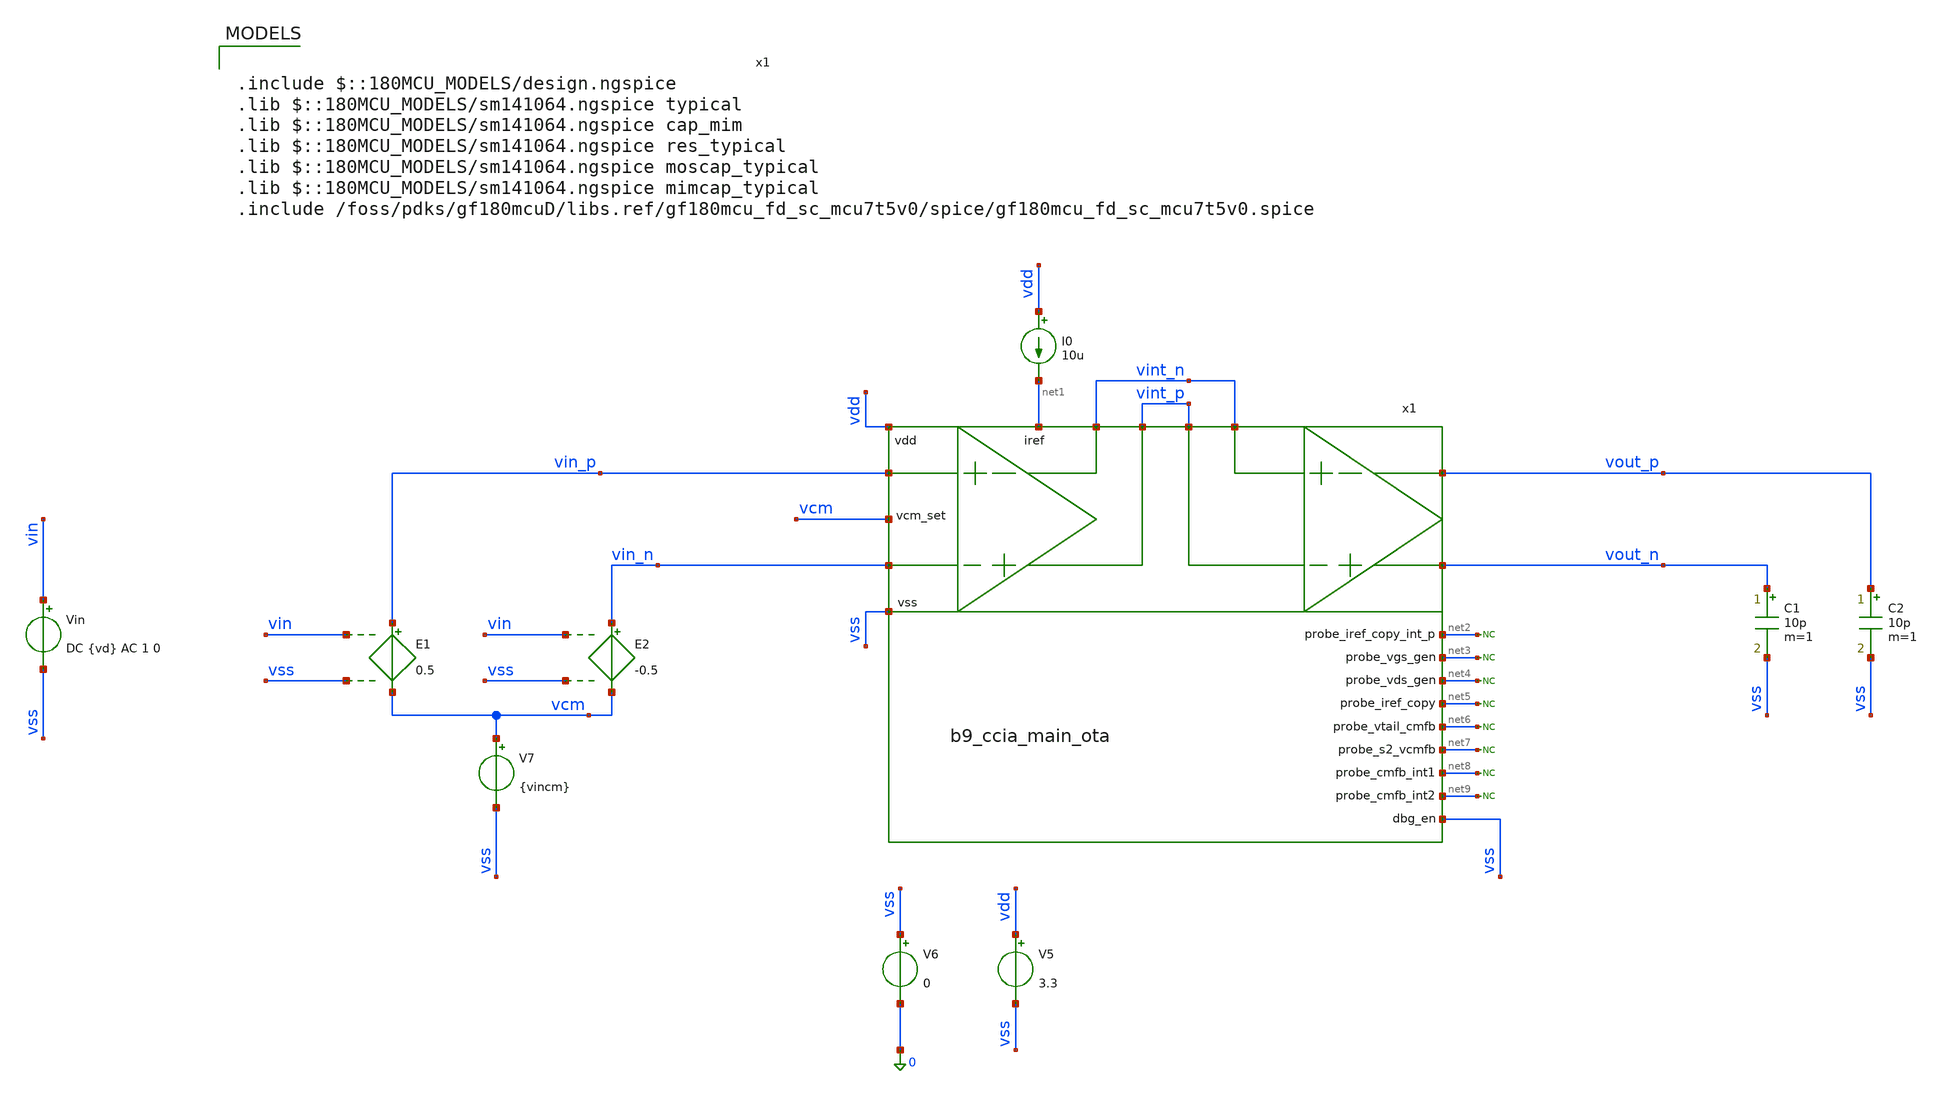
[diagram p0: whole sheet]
** sch_path: xschem/ccia_main_ota/b9_ccia_main_ota_tb_basic.sch
**.subckt b9_ccia_main_ota_tb_basic
I0 vdd net1 10u
C1 vout_n vss 10p m=1
C2 vout_p vss 10p m=1
V7 vcm vss {vincm}
E1 vin_p vcm vin vss 0.5
E2 vin_n vcm vin vss -0.5
Vin vin vss DC {vd} AC 1 0
V5 vdd vss 3.3
V6 vss 0 0
x1 net2 net3 net4 net5 net6 net7 net8 net9 vss net1 vdd vint_p vin_p vin_n vint_n vss vout_n vint_n
+ vcm vint_p vout_p b9_ccia_main_ota
* noconn #net2
* noconn #net3
* noconn #net4
* noconn #net5
* noconn #net6
* noconn #net7
* noconn #net8
* noconn #net9
**** begin user architecture code

.include $::180MCU_MODELS/design.ngspice
.lib $::180MCU_MODELS/sm141064.ngspice typical
.lib $::180MCU_MODELS/sm141064.ngspice cap_mim
.lib $::180MCU_MODELS/sm141064.ngspice res_typical
.lib $::180MCU_MODELS/sm141064.ngspice moscap_typical
.lib $::180MCU_MODELS/sm141064.ngspice mimcap_typical
.include /foss/pdks/gf180mcuD/libs.ref/gf180mcu_fd_sc_mcu7t5v0/spice/gf180mcu_fd_sc_mcu7t5v0.spice


.param vincm=1
.param voutcm=0.8
.param vd=0
.control
save all
save @m.x1.x10.x1.xm1.m0[id] @m.x1.x10.x1.xm1.m0[gm] @m.x1.x10.x1.xm1.m0[gds]
+ @m.x1.x10.x1.xm1.m0[cdb] @m.x1.x10.x1.xm1.m0[cgs] @m.x1.x10.x1.xm1.m0[csb] @m.x1.x10.x1.xm1.m0[cgd]
save @m.x1.x10.x1.xm2.m0[id] @m.x1.x10.x1.xm2.m0[gm] @m.x1.x10.x1.xm2.m0[gds]
+ @m.x1.x10.x1.xm2.m0[cdb] @m.x1.x10.x1.xm2.m0[cgs] @m.x1.x10.x1.xm2.m0[csb] @m.x1.x10.x1.xm2.m0[cgd]
save @m.x1.x10.xm1.m0[id] @m.x1.x10.xm1.m0[gm] @m.x1.x10.xm1.m0[gds] @m.x1.x10.xm1.m0[cdb]
+ @m.x1.x10.xm1.m0[cgs] @m.x1.x10.xm1.m0[csb] @m.x1.x10.xm1.m0[cgd]
save @m.x1.x12.x1.xm1.m0[id] @m.x1.x12.x1.xm1.m0[gm] @m.x1.x12.x1.xm1.m0[gds]
+ @m.x1.x12.x1.xm1.m0[cdb] @m.x1.x12.x1.xm1.m0[cgs] @m.x1.x12.x1.xm1.m0[csb] @m.x1.x12.x1.xm1.m0[cgd]
save @m.x1.x12.x1.xm2.m0[id] @m.x1.x12.x1.xm2.m0[gm] @m.x1.x12.x1.xm2.m0[gds]
+ @m.x1.x12.x1.xm2.m0[cdb] @m.x1.x12.x1.xm2.m0[cgs] @m.x1.x12.x1.xm2.m0[csb] @m.x1.x12.x1.xm2.m0[cgd]
save @m.x1.x12.xm1.m0[id] @m.x1.x12.xm1.m0[gm] @m.x1.x12.xm1.m0[gds] @m.x1.x12.xm1.m0[cdb]
+ @m.x1.x12.xm1.m0[cgs] @m.x1.x12.xm1.m0[csb] @m.x1.x12.xm1.m0[cgd]
save @m.x1.x15.m0[id] @m.x1.x15.m0[gm] @m.x1.x15.m0[gds] @m.x1.x15.m0[cdb] @m.x1.x15.m0[cgs]
+ @m.x1.x15.m0[csb] @m.x1.x15.m0[cgd]
save @m.x1.x13.x1.xm1.m0[id] @m.x1.x13.x1.xm1.m0[gm] @m.x1.x13.x1.xm1.m0[gds]
+ @m.x1.x13.x1.xm1.m0[cdb] @m.x1.x13.x1.xm1.m0[cgs] @m.x1.x13.x1.xm1.m0[csb] @m.x1.x13.x1.xm1.m0[cgd]
save @m.x1.x13.x1.xm2.m0[id] @m.x1.x13.x1.xm2.m0[gm] @m.x1.x13.x1.xm2.m0[gds]
+ @m.x1.x13.x1.xm2.m0[cdb] @m.x1.x13.x1.xm2.m0[cgs] @m.x1.x13.x1.xm2.m0[csb] @m.x1.x13.x1.xm2.m0[cgd]
save @m.x1.x13.xm1.m0[id] @m.x1.x13.xm1.m0[gm] @m.x1.x13.xm1.m0[gds] @m.x1.x13.xm1.m0[cdb]
+ @m.x1.x13.xm1.m0[cgs] @m.x1.x13.xm1.m0[csb] @m.x1.x13.xm1.m0[cgd]
save @m.x1.x14.x1.xm1.m0[id] @m.x1.x14.x1.xm1.m0[gm] @m.x1.x14.x1.xm1.m0[gds]
+ @m.x1.x14.x1.xm1.m0[cdb] @m.x1.x14.x1.xm1.m0[cgs] @m.x1.x14.x1.xm1.m0[csb] @m.x1.x14.x1.xm1.m0[cgd]
save @m.x1.x14.x1.xm2.m0[id] @m.x1.x14.x1.xm2.m0[gm] @m.x1.x14.x1.xm2.m0[gds]
+ @m.x1.x14.x1.xm2.m0[cdb] @m.x1.x14.x1.xm2.m0[cgs] @m.x1.x14.x1.xm2.m0[csb] @m.x1.x14.x1.xm2.m0[cgd]
save @m.x1.x14.xm1.m0[id] @m.x1.x14.xm1.m0[gm] @m.x1.x14.xm1.m0[gds] @m.x1.x14.xm1.m0[cdb]
+ @m.x1.x14.xm1.m0[cgs] @m.x1.x14.xm1.m0[csb] @m.x1.x14.xm1.m0[cgd]
save @m.x1.x16.x1.xm1.m0[id] @m.x1.x16.x1.xm1.m0[gm] @m.x1.x16.x1.xm1.m0[gds]
+ @m.x1.x16.x1.xm1.m0[cdb] @m.x1.x16.x1.xm1.m0[cgs] @m.x1.x16.x1.xm1.m0[csb] @m.x1.x16.x1.xm1.m0[cgd]
save @m.x1.x16.x1.xm2.m0[id] @m.x1.x16.x1.xm2.m0[gm] @m.x1.x16.x1.xm2.m0[gds]
+ @m.x1.x16.x1.xm2.m0[cdb] @m.x1.x16.x1.xm2.m0[cgs] @m.x1.x16.x1.xm2.m0[csb] @m.x1.x16.x1.xm2.m0[cgd]
save @m.x1.x16.xm1.m0[id] @m.x1.x16.xm1.m0[gm] @m.x1.x16.xm1.m0[gds] @m.x1.x16.xm1.m0[cdb]
+ @m.x1.x16.xm1.m0[cgs] @m.x1.x16.xm1.m0[csb] @m.x1.x16.xm1.m0[cgd]
save @m.x1.x17.x1.xm1.m0[id] @m.x1.x17.x1.xm1.m0[gm] @m.x1.x17.x1.xm1.m0[gds]
+ @m.x1.x17.x1.xm1.m0[cdb] @m.x1.x17.x1.xm1.m0[cgs] @m.x1.x17.x1.xm1.m0[csb] @m.x1.x17.x1.xm1.m0[cgd]
save @m.x1.x17.x1.xm2.m0[id] @m.x1.x17.x1.xm2.m0[gm] @m.x1.x17.x1.xm2.m0[gds]
+ @m.x1.x17.x1.xm2.m0[cdb] @m.x1.x17.x1.xm2.m0[cgs] @m.x1.x17.x1.xm2.m0[csb] @m.x1.x17.x1.xm2.m0[cgd]
save @m.x1.x17.xm1.m0[id] @m.x1.x17.xm1.m0[gm] @m.x1.x17.xm1.m0[gds] @m.x1.x17.xm1.m0[cdb]
+ @m.x1.x17.xm1.m0[cgs] @m.x1.x17.xm1.m0[csb] @m.x1.x17.xm1.m0[cgd]
save @m.x1.x18.x1.xm1.m0[id] @m.x1.x18.x1.xm1.m0[gm] @m.x1.x18.x1.xm1.m0[gds]
+ @m.x1.x18.x1.xm1.m0[cdb] @m.x1.x18.x1.xm1.m0[cgs] @m.x1.x18.x1.xm1.m0[csb] @m.x1.x18.x1.xm1.m0[cgd]
save @m.x1.x18.x1.xm2.m0[id] @m.x1.x18.x1.xm2.m0[gm] @m.x1.x18.x1.xm2.m0[gds]
+ @m.x1.x18.x1.xm2.m0[cdb] @m.x1.x18.x1.xm2.m0[cgs] @m.x1.x18.x1.xm2.m0[csb] @m.x1.x18.x1.xm2.m0[cgd]
save @m.x1.x18.xm1.m0[id] @m.x1.x18.xm1.m0[gm] @m.x1.x18.xm1.m0[gds] @m.x1.x18.xm1.m0[cdb]
+ @m.x1.x18.xm1.m0[cgs] @m.x1.x18.xm1.m0[csb] @m.x1.x18.xm1.m0[cgd]
save @m.x1.x19.x1.xm1.m0[id] @m.x1.x19.x1.xm1.m0[gm] @m.x1.x19.x1.xm1.m0[gds]
+ @m.x1.x19.x1.xm1.m0[cdb] @m.x1.x19.x1.xm1.m0[cgs] @m.x1.x19.x1.xm1.m0[csb] @m.x1.x19.x1.xm1.m0[cgd]
save @m.x1.x19.x1.xm2.m0[id] @m.x1.x19.x1.xm2.m0[gm] @m.x1.x19.x1.xm2.m0[gds]
+ @m.x1.x19.x1.xm2.m0[cdb] @m.x1.x19.x1.xm2.m0[cgs] @m.x1.x19.x1.xm2.m0[csb] @m.x1.x19.x1.xm2.m0[cgd]
save @m.x1.x19.xm1.m0[id] @m.x1.x19.xm1.m0[gm] @m.x1.x19.xm1.m0[gds] @m.x1.x19.xm1.m0[cdb]
+ @m.x1.x19.xm1.m0[cgs] @m.x1.x19.xm1.m0[csb] @m.x1.x19.xm1.m0[cgd]
save @m.x1.x2.xm1.m0[id] @m.x1.x2.xm1.m0[gm] @m.x1.x2.xm1.m0[gds] @m.x1.x2.xm1.m0[cdb]
+ @m.x1.x2.xm1.m0[cgs] @m.x1.x2.xm1.m0[csb] @m.x1.x2.xm1.m0[cgd]
save @m.x1.x2.xm7.m0[id] @m.x1.x2.xm7.m0[gm] @m.x1.x2.xm7.m0[gds] @m.x1.x2.xm7.m0[cdb]
+ @m.x1.x2.xm7.m0[cgs] @m.x1.x2.xm7.m0[csb] @m.x1.x2.xm7.m0[cgd]
save @m.x1.x2.xm17.m0[id] @m.x1.x2.xm17.m0[gm] @m.x1.x2.xm17.m0[gds] @m.x1.x2.xm17.m0[cdb]
+ @m.x1.x2.xm17.m0[cgs] @m.x1.x2.xm17.m0[csb] @m.x1.x2.xm17.m0[cgd]
save @m.x1.x2.xm18.m0[id] @m.x1.x2.xm18.m0[gm] @m.x1.x2.xm18.m0[gds] @m.x1.x2.xm18.m0[cdb]
+ @m.x1.x2.xm18.m0[cgs] @m.x1.x2.xm18.m0[csb] @m.x1.x2.xm18.m0[cgd]
save @m.x1.x2.xm4.m0[id] @m.x1.x2.xm4.m0[gm] @m.x1.x2.xm4.m0[gds] @m.x1.x2.xm4.m0[cdb]
+ @m.x1.x2.xm4.m0[cgs] @m.x1.x2.xm4.m0[csb] @m.x1.x2.xm4.m0[cgd]
save @m.x1.x2.xm16.m0[id] @m.x1.x2.xm16.m0[gm] @m.x1.x2.xm16.m0[gds] @m.x1.x2.xm16.m0[cdb]
+ @m.x1.x2.xm16.m0[cgs] @m.x1.x2.xm16.m0[csb] @m.x1.x2.xm16.m0[cgd]
save @m.x1.x2.xm19.m0[id] @m.x1.x2.xm19.m0[gm] @m.x1.x2.xm19.m0[gds] @m.x1.x2.xm19.m0[cdb]
+ @m.x1.x2.xm19.m0[cgs] @m.x1.x2.xm19.m0[csb] @m.x1.x2.xm19.m0[cgd]
save @m.x1.x2.xm11.m0[id] @m.x1.x2.xm11.m0[gm] @m.x1.x2.xm11.m0[gds] @m.x1.x2.xm11.m0[cdb]
+ @m.x1.x2.xm11.m0[cgs] @m.x1.x2.xm11.m0[csb] @m.x1.x2.xm11.m0[cgd]
save @m.x1.x2.xm6.m0[id] @m.x1.x2.xm6.m0[gm] @m.x1.x2.xm6.m0[gds] @m.x1.x2.xm6.m0[cdb]
+ @m.x1.x2.xm6.m0[cgs] @m.x1.x2.xm6.m0[csb] @m.x1.x2.xm6.m0[cgd]
save @m.x1.x2.xm25.m0[id] @m.x1.x2.xm25.m0[gm] @m.x1.x2.xm25.m0[gds] @m.x1.x2.xm25.m0[cdb]
+ @m.x1.x2.xm25.m0[cgs] @m.x1.x2.xm25.m0[csb] @m.x1.x2.xm25.m0[cgd]
save @m.x1.x2.xm26.m0[id] @m.x1.x2.xm26.m0[gm] @m.x1.x2.xm26.m0[gds] @m.x1.x2.xm26.m0[cdb]
+ @m.x1.x2.xm26.m0[cgs] @m.x1.x2.xm26.m0[csb] @m.x1.x2.xm26.m0[cgd]
save @m.x1.x2.xm27.m0[id] @m.x1.x2.xm27.m0[gm] @m.x1.x2.xm27.m0[gds] @m.x1.x2.xm27.m0[cdb]
+ @m.x1.x2.xm27.m0[cgs] @m.x1.x2.xm27.m0[csb] @m.x1.x2.xm27.m0[cgd]
save @m.x1.x5.xm1.m0[id] @m.x1.x5.xm1.m0[gm] @m.x1.x5.xm1.m0[gds] @m.x1.x5.xm1.m0[cdb]
+ @m.x1.x5.xm1.m0[cgs] @m.x1.x5.xm1.m0[csb] @m.x1.x5.xm1.m0[cgd]
save @m.x1.x5.xm2.m0[id] @m.x1.x5.xm2.m0[gm] @m.x1.x5.xm2.m0[gds] @m.x1.x5.xm2.m0[cdb]
+ @m.x1.x5.xm2.m0[cgs] @m.x1.x5.xm2.m0[csb] @m.x1.x5.xm2.m0[cgd]
save @m.x1.x1.xm2.m0[id] @m.x1.x1.xm2.m0[gm] @m.x1.x1.xm2.m0[gds] @m.x1.x1.xm2.m0[cdb]
+ @m.x1.x1.xm2.m0[cgs] @m.x1.x1.xm2.m0[csb] @m.x1.x1.xm2.m0[cgd]
save @m.x1.x1.xm1.m0[id] @m.x1.x1.xm1.m0[gm] @m.x1.x1.xm1.m0[gds] @m.x1.x1.xm1.m0[cdb]
+ @m.x1.x1.xm1.m0[cgs] @m.x1.x1.xm1.m0[csb] @m.x1.x1.xm1.m0[cgd]
save @m.x1.x4.xm9.m0[id] @m.x1.x4.xm9.m0[gm] @m.x1.x4.xm9.m0[gds] @m.x1.x4.xm9.m0[cdb]
+ @m.x1.x4.xm9.m0[cgs] @m.x1.x4.xm9.m0[csb] @m.x1.x4.xm9.m0[cgd]
save @m.x1.x4.xm22.m0[id] @m.x1.x4.xm22.m0[gm] @m.x1.x4.xm22.m0[gds] @m.x1.x4.xm22.m0[cdb]
+ @m.x1.x4.xm22.m0[cgs] @m.x1.x4.xm22.m0[csb] @m.x1.x4.xm22.m0[cgd]
save @m.x1.x4.xm21.m0[id] @m.x1.x4.xm21.m0[gm] @m.x1.x4.xm21.m0[gds] @m.x1.x4.xm21.m0[cdb]
+ @m.x1.x4.xm21.m0[cgs] @m.x1.x4.xm21.m0[csb] @m.x1.x4.xm21.m0[cgd]
save @m.x1.x4.xm8.m0[id] @m.x1.x4.xm8.m0[gm] @m.x1.x4.xm8.m0[gds] @m.x1.x4.xm8.m0[cdb]
+ @m.x1.x4.xm8.m0[cgs] @m.x1.x4.xm8.m0[csb] @m.x1.x4.xm8.m0[cgd]
save @m.x1.x4.xm20.m0[id] @m.x1.x4.xm20.m0[gm] @m.x1.x4.xm20.m0[gds] @m.x1.x4.xm20.m0[cdb]
+ @m.x1.x4.xm20.m0[cgs] @m.x1.x4.xm20.m0[csb] @m.x1.x4.xm20.m0[cgd]
save @m.x1.x3.xm14.m0[id] @m.x1.x3.xm14.m0[gm] @m.x1.x3.xm14.m0[gds] @m.x1.x3.xm14.m0[cdb]
+ @m.x1.x3.xm14.m0[cgs] @m.x1.x3.xm14.m0[csb] @m.x1.x3.xm14.m0[cgd]
save @m.x1.x3.xm15.m0[id] @m.x1.x3.xm15.m0[gm] @m.x1.x3.xm15.m0[gds] @m.x1.x3.xm15.m0[cdb]
+ @m.x1.x3.xm15.m0[cgs] @m.x1.x3.xm15.m0[csb] @m.x1.x3.xm15.m0[cgd]
save @m.x1.x3.xm10.m0[id] @m.x1.x3.xm10.m0[gm] @m.x1.x3.xm10.m0[gds] @m.x1.x3.xm10.m0[cdb]
+ @m.x1.x3.xm10.m0[cgs] @m.x1.x3.xm10.m0[csb] @m.x1.x3.xm10.m0[cgd]
save @m.x1.x3.xm5.m0[id] @m.x1.x3.xm5.m0[gm] @m.x1.x3.xm5.m0[gds] @m.x1.x3.xm5.m0[cdb]
+ @m.x1.x3.xm5.m0[cgs] @m.x1.x3.xm5.m0[csb] @m.x1.x3.xm5.m0[cgd]
save @m.x1.x3.xm23.m0[id] @m.x1.x3.xm23.m0[gm] @m.x1.x3.xm23.m0[gds] @m.x1.x3.xm23.m0[cdb]
+ @m.x1.x3.xm23.m0[cgs] @m.x1.x3.xm23.m0[csb] @m.x1.x3.xm23.m0[cgd]
save @m.x1.x3.xm24.m0[id] @m.x1.x3.xm24.m0[gm] @m.x1.x3.xm24.m0[gds] @m.x1.x3.xm24.m0[cdb]
+ @m.x1.x3.xm24.m0[cgs] @m.x1.x3.xm24.m0[csb] @m.x1.x3.xm24.m0[cgd]
save @m.x1.x7.xm6.m0[id] @m.x1.x7.xm6.m0[gm] @m.x1.x7.xm6.m0[gds] @m.x1.x7.xm6.m0[cdb]
+ @m.x1.x7.xm6.m0[cgs] @m.x1.x7.xm6.m0[csb] @m.x1.x7.xm6.m0[cgd]
save @m.x1.x7.xm1.m0[id] @m.x1.x7.xm1.m0[gm] @m.x1.x7.xm1.m0[gds] @m.x1.x7.xm1.m0[cdb]
+ @m.x1.x7.xm1.m0[cgs] @m.x1.x7.xm1.m0[csb] @m.x1.x7.xm1.m0[cgd]
save @m.x1.x8.xm6.m0[id] @m.x1.x8.xm6.m0[gm] @m.x1.x8.xm6.m0[gds] @m.x1.x8.xm6.m0[cdb]
+ @m.x1.x8.xm6.m0[cgs] @m.x1.x8.xm6.m0[csb] @m.x1.x8.xm6.m0[cgd]
save @m.x1.x8.xm1.m0[id] @m.x1.x8.xm1.m0[gm] @m.x1.x8.xm1.m0[gds] @m.x1.x8.xm1.m0[cdb]
+ @m.x1.x8.xm1.m0[cgs] @m.x1.x8.xm1.m0[csb] @m.x1.x8.xm1.m0[cgd]
save @m.x1.x6.xm15.m0[id] @m.x1.x6.xm15.m0[gm] @m.x1.x6.xm15.m0[gds] @m.x1.x6.xm15.m0[cdb]
+ @m.x1.x6.xm15.m0[cgs] @m.x1.x6.xm15.m0[csb] @m.x1.x6.xm15.m0[cgd]
save @m.x1.x6.xm1.m0[id] @m.x1.x6.xm1.m0[gm] @m.x1.x6.xm1.m0[gds] @m.x1.x6.xm1.m0[cdb]
+ @m.x1.x6.xm1.m0[cgs] @m.x1.x6.xm1.m0[csb] @m.x1.x6.xm1.m0[cgd]
save @m.x1.x6.xm2.m0[id] @m.x1.x6.xm2.m0[gm] @m.x1.x6.xm2.m0[gds] @m.x1.x6.xm2.m0[cdb]
+ @m.x1.x6.xm2.m0[cgs] @m.x1.x6.xm2.m0[csb] @m.x1.x6.xm2.m0[cgd]
save @m.x1.x6.xm7.m0[id] @m.x1.x6.xm7.m0[gm] @m.x1.x6.xm7.m0[gds] @m.x1.x6.xm7.m0[cdb]
+ @m.x1.x6.xm7.m0[cgs] @m.x1.x6.xm7.m0[csb] @m.x1.x6.xm7.m0[cgd]
save @m.x1.x6.xm8.m0[id] @m.x1.x6.xm8.m0[gm] @m.x1.x6.xm8.m0[gds] @m.x1.x6.xm8.m0[cdb]
+ @m.x1.x6.xm8.m0[cgs] @m.x1.x6.xm8.m0[csb] @m.x1.x6.xm8.m0[cgd]
save @m.x1.x6.xm4.m0[id] @m.x1.x6.xm4.m0[gm] @m.x1.x6.xm4.m0[gds] @m.x1.x6.xm4.m0[cdb]
+ @m.x1.x6.xm4.m0[cgs] @m.x1.x6.xm4.m0[csb] @m.x1.x6.xm4.m0[cgd]
save @m.x1.x6.xm3.m0[id] @m.x1.x6.xm3.m0[gm] @m.x1.x6.xm3.m0[gds] @m.x1.x6.xm3.m0[cdb]
+ @m.x1.x6.xm3.m0[cgs] @m.x1.x6.xm3.m0[csb] @m.x1.x6.xm3.m0[cgd]
save @m.x1.x6.xm5.m0[id] @m.x1.x6.xm5.m0[gm] @m.x1.x6.xm5.m0[gds] @m.x1.x6.xm5.m0[cdb]
+ @m.x1.x6.xm5.m0[cgs] @m.x1.x6.xm5.m0[csb] @m.x1.x6.xm5.m0[cgd]
save @m.x1.x6.xm6.m0[id] @m.x1.x6.xm6.m0[gm] @m.x1.x6.xm6.m0[gds] @m.x1.x6.xm6.m0[cdb]
+ @m.x1.x6.xm6.m0[cgs] @m.x1.x6.xm6.m0[csb] @m.x1.x6.xm6.m0[cgd]

op
write ota_op.raw all
ac dec 100 1 10G
write ota_ac.raw all
.endc


**** end user architecture code
**.ends
.end
